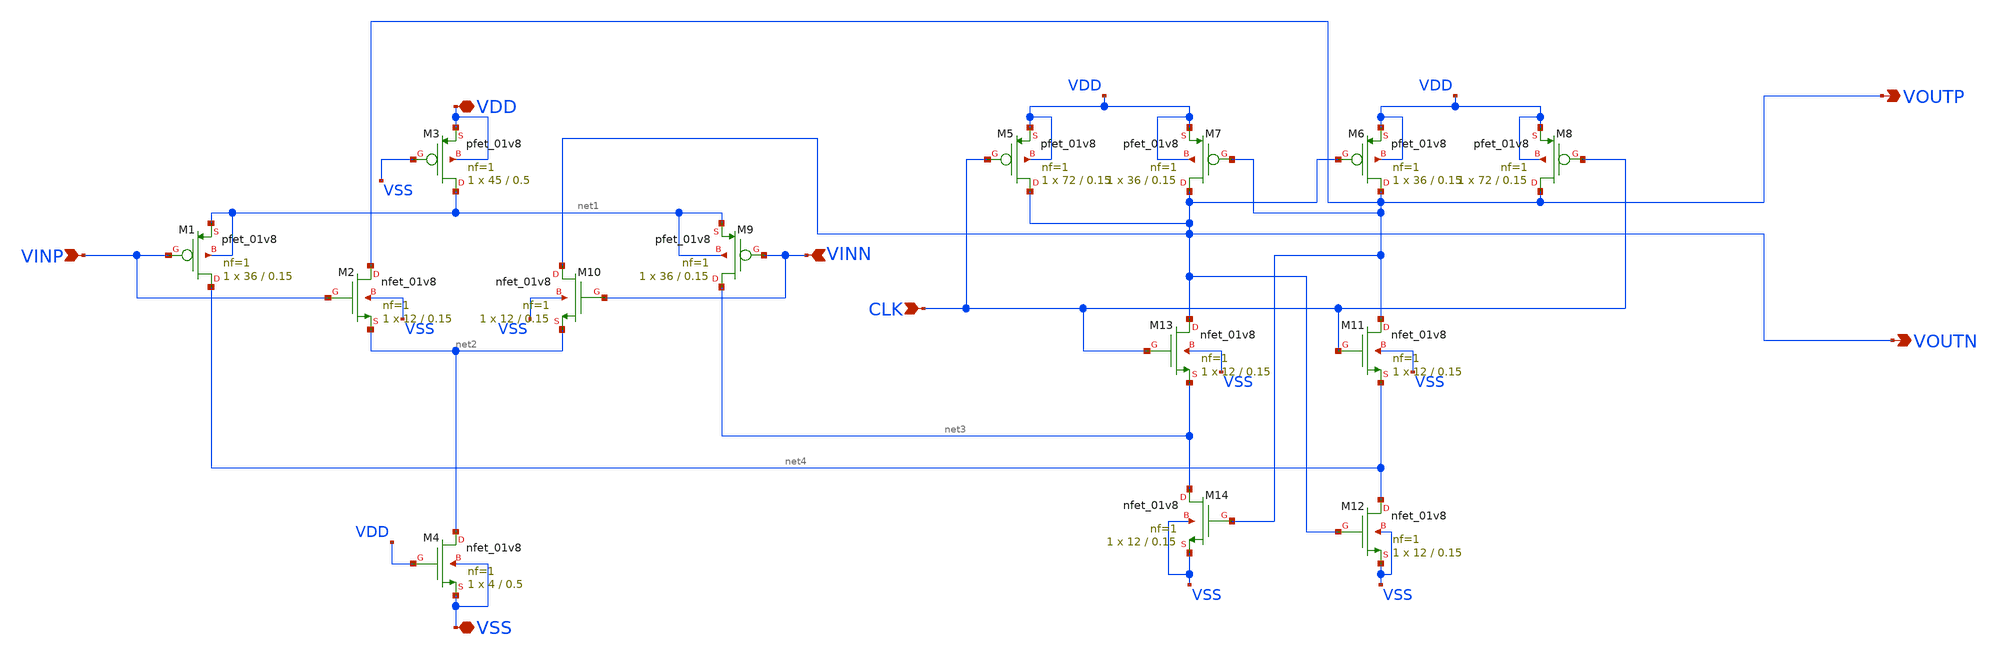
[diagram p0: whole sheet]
** sch_path: SKY130/SAR-ADC/SAR-ADC_1.8V/comp.sch
**.subckt comp VOUTP VOUTN VINP VINN CLK VDD VSS
*.opin VOUTP
*.opin VOUTN
*.ipin VINP
*.ipin VINN
*.ipin CLK
*.iopin VDD
*.iopin VSS
XM1 net4 VINP net1 net1 sky130_fd_pr__pfet_01v8 L=0.15 W=36 nf=1 ad='int((nf+1)/2) * W/nf * 0.29' as='int((nf+2)/2) * W/nf * 0.29'
+ pd='2*int((nf+1)/2) * (W/nf + 0.29)' ps='2*int((nf+2)/2) * (W/nf + 0.29)' nrd='0.29 / W' nrs='0.29 / W'
+ sa=0 sb=0 sd=0 mult=1 m=1
XM3 net1 VSS VDD VDD sky130_fd_pr__pfet_01v8 L=0.5 W=45 nf=1 ad='int((nf+1)/2) * W/nf * 0.29' as='int((nf+2)/2) * W/nf * 0.29'
+ pd='2*int((nf+1)/2) * (W/nf + 0.29)' ps='2*int((nf+2)/2) * (W/nf + 0.29)' nrd='0.29 / W' nrs='0.29 / W'
+ sa=0 sb=0 sd=0 mult=1 m=1
XM9 net3 VINN net1 net1 sky130_fd_pr__pfet_01v8 L=0.15 W=36 nf=1 ad='int((nf+1)/2) * W/nf * 0.29' as='int((nf+2)/2) * W/nf * 0.29'
+ pd='2*int((nf+1)/2) * (W/nf + 0.29)' ps='2*int((nf+2)/2) * (W/nf + 0.29)' nrd='0.29 / W' nrs='0.29 / W'
+ sa=0 sb=0 sd=0 mult=1 m=1
XM4 net2 VDD VSS VSS sky130_fd_pr__nfet_01v8 L=0.5 W=4 nf=1 ad='int((1 + 1)/2) * 4 / 1 * 0.29' as='int((1 + 2)/2) * 4 / 1 * 0.29'
+ pd='2*int((1 + 1)/2) * (4 / 1 + 0.29)' ps='2*int((1 + 2)/2) * (4 / 1 + 0.29)' nrd='0.29 / 4 ' nrs='0.29 / 4 '
+ sa=0 sb=0 sd=0 mult=1 m=1
XM5 VOUTN CLK VDD VDD sky130_fd_pr__pfet_01v8 L=0.15 W=72 nf=1 ad='int((nf+1)/2) * W/nf * 0.29' as='int((nf+2)/2) * W/nf * 0.29'
+ pd='2*int((nf+1)/2) * (W/nf + 0.29)' ps='2*int((nf+2)/2) * (W/nf + 0.29)' nrd='0.29 / W' nrs='0.29 / W'
+ sa=0 sb=0 sd=0 mult=1 m=1
XM6 VOUTP VOUTN VDD VDD sky130_fd_pr__pfet_01v8 L=0.15 W=36 nf=1 ad='int((nf+1)/2) * W/nf * 0.29' as='int((nf+2)/2) * W/nf * 0.29'
+ pd='2*int((nf+1)/2) * (W/nf + 0.29)' ps='2*int((nf+2)/2) * (W/nf + 0.29)' nrd='0.29 / W' nrs='0.29 / W'
+ sa=0 sb=0 sd=0 mult=1 m=1
XM7 VOUTN VOUTP VDD VDD sky130_fd_pr__pfet_01v8 L=0.15 W=36 nf=1 ad='int((nf+1)/2) * W/nf * 0.29' as='int((nf+2)/2) * W/nf * 0.29'
+ pd='2*int((nf+1)/2) * (W/nf + 0.29)' ps='2*int((nf+2)/2) * (W/nf + 0.29)' nrd='0.29 / W' nrs='0.29 / W'
+ sa=0 sb=0 sd=0 mult=1 m=1
XM8 VOUTP CLK VDD VDD sky130_fd_pr__pfet_01v8 L=0.15 W=72 nf=1 ad='int((nf+1)/2) * W/nf * 0.29' as='int((nf+2)/2) * W/nf * 0.29'
+ pd='2*int((nf+1)/2) * (W/nf + 0.29)' ps='2*int((nf+2)/2) * (W/nf + 0.29)' nrd='0.29 / W' nrs='0.29 / W'
+ sa=0 sb=0 sd=0 mult=1 m=1
XM11 VOUTP CLK net4 VSS sky130_fd_pr__nfet_01v8 L=0.15 W=12 nf=1 ad='int((1 + 1)/2) * 12 / 1 * 0.29'
+ as='int((1 + 2)/2) * 12 / 1 * 0.29' pd='2*int((1 + 1)/2) * (12 / 1 + 0.29)' ps='2*int((1 + 2)/2) * (12 / 1 + 0.29)'
+ nrd='0.29 / 12 ' nrs='0.29 / 12 ' sa=0 sb=0 sd=0 mult=1 m=1
XM12 net4 VOUTN VSS VSS sky130_fd_pr__nfet_01v8 L=0.15 W=12 nf=1 ad='int((1 + 1)/2) * 12 / 1 * 0.29'
+ as='int((1 + 2)/2) * 12 / 1 * 0.29' pd='2*int((1 + 1)/2) * (12 / 1 + 0.29)' ps='2*int((1 + 2)/2) * (12 / 1 + 0.29)'
+ nrd='0.29 / 12 ' nrs='0.29 / 12 ' sa=0 sb=0 sd=0 mult=1 m=1
XM13 VOUTN CLK net3 VSS sky130_fd_pr__nfet_01v8 L=0.15 W=12 nf=1 ad='int((1 + 1)/2) * 12 / 1 * 0.29'
+ as='int((1 + 2)/2) * 12 / 1 * 0.29' pd='2*int((1 + 1)/2) * (12 / 1 + 0.29)' ps='2*int((1 + 2)/2) * (12 / 1 + 0.29)'
+ nrd='0.29 / 12 ' nrs='0.29 / 12 ' sa=0 sb=0 sd=0 mult=1 m=1
XM14 net3 VOUTP VSS VSS sky130_fd_pr__nfet_01v8 L=0.15 W=12 nf=1 ad='int((1 + 1)/2) * 12 / 1 * 0.29'
+ as='int((1 + 2)/2) * 12 / 1 * 0.29' pd='2*int((1 + 1)/2) * (12 / 1 + 0.29)' ps='2*int((1 + 2)/2) * (12 / 1 + 0.29)'
+ nrd='0.29 / 12 ' nrs='0.29 / 12 ' sa=0 sb=0 sd=0 mult=1 m=1
XM2 VOUTP VINP net2 VSS sky130_fd_pr__nfet_01v8 L=0.15 W=12 nf=1 ad='int((1 + 1)/2) * 12 / 1 * 0.29'
+ as='int((1 + 2)/2) * 12 / 1 * 0.29' pd='2*int((1 + 1)/2) * (12 / 1 + 0.29)' ps='2*int((1 + 2)/2) * (12 / 1 + 0.29)'
+ nrd='0.29 / 12 ' nrs='0.29 / 12 ' sa=0 sb=0 sd=0 mult=1 m=1
XM10 VOUTN VINN net2 VSS sky130_fd_pr__nfet_01v8 L=0.15 W=12 nf=1 ad='int((1 + 1)/2) * 12 / 1 * 0.29'
+ as='int((1 + 2)/2) * 12 / 1 * 0.29' pd='2*int((1 + 1)/2) * (12 / 1 + 0.29)' ps='2*int((1 + 2)/2) * (12 / 1 + 0.29)'
+ nrd='0.29 / 12 ' nrs='0.29 / 12 ' sa=0 sb=0 sd=0 mult=1 m=1
**.ends
.end
